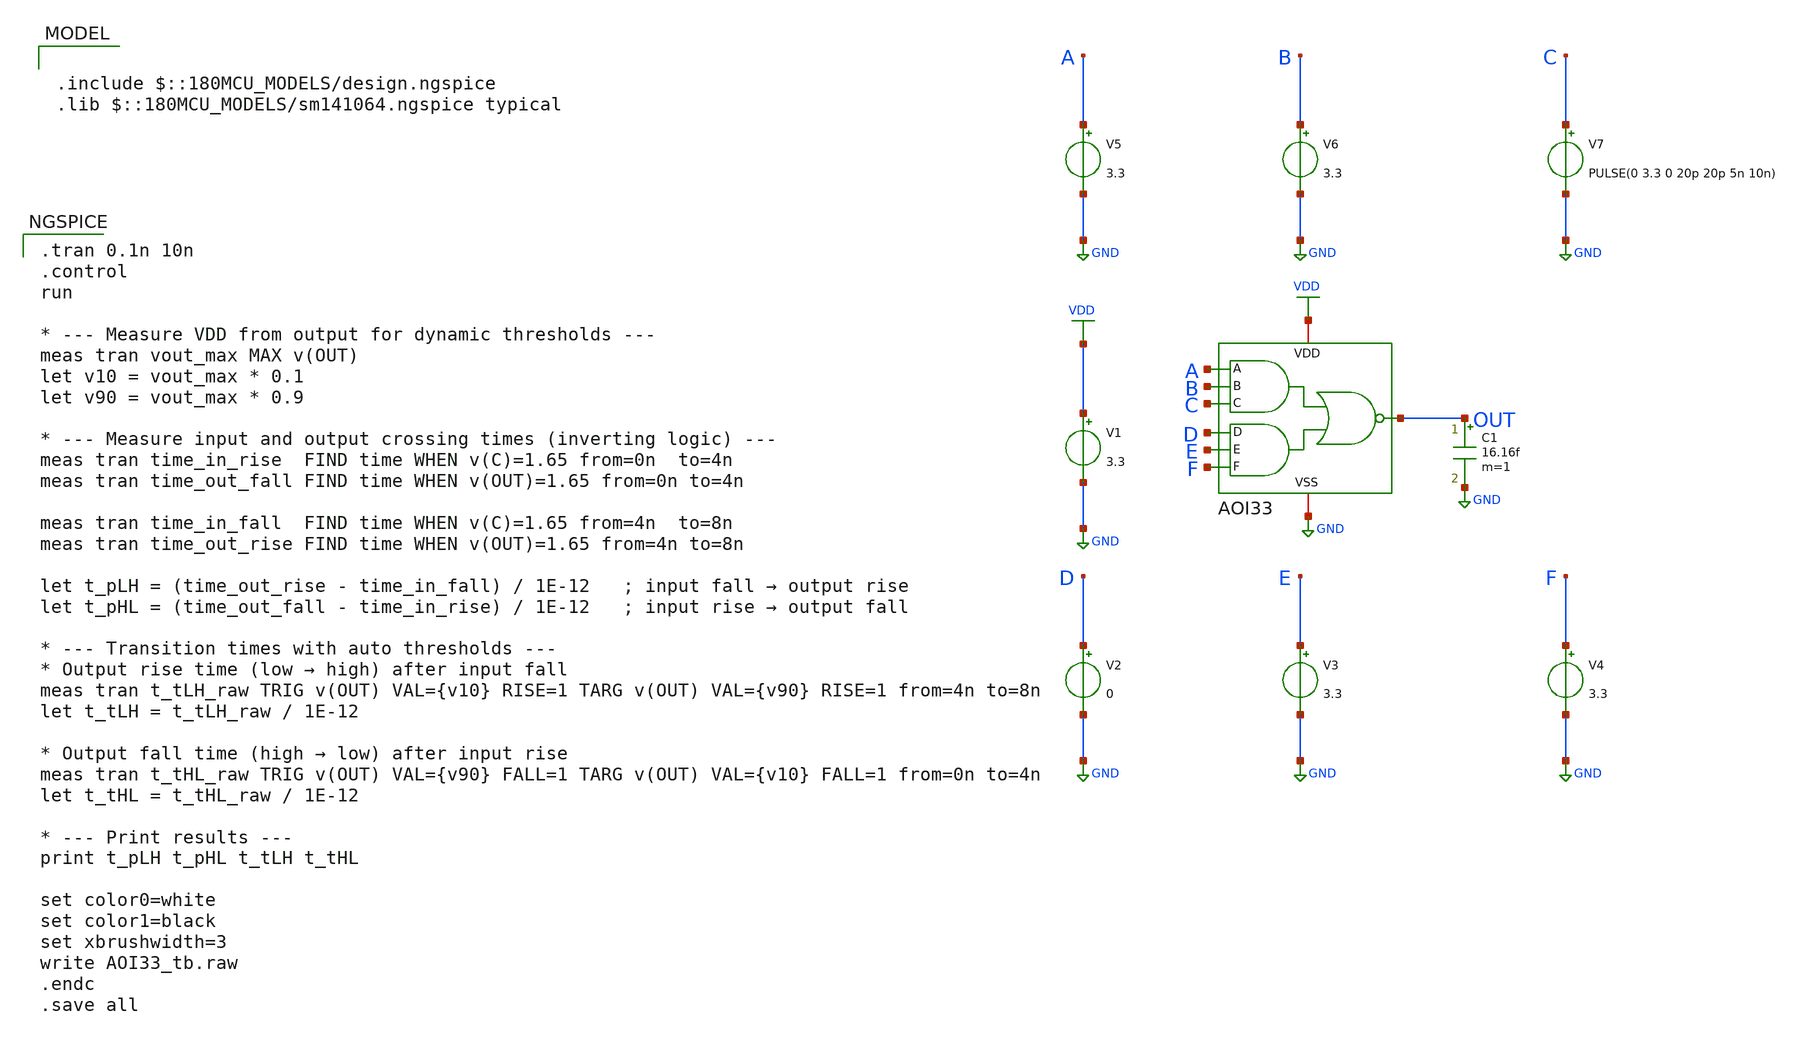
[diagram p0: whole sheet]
** sch_path: designs/AOI33/xschem/AOI33_tb.sch
**.subckt AOI33_tb
V1 VDD GND 3.3
V2 D GND 0
V3 E GND 3.3
V4 F GND 3.3
V5 A GND 3.3
V6 B GND 3.3
V7 C GND PULSE(0 3.3 0 20p 20p 5n 10n)
C1 OUT GND 16.16f m=1
x1 VDD C B A F E D OUT GND AOI33
**** begin user architecture code

.include $::180MCU_MODELS/design.ngspice
.lib $::180MCU_MODELS/sm141064.ngspice typical


.tran 0.1n 10n
.control
run

* --- Measure VDD from output for dynamic thresholds ---
meas tran vout_max MAX v(OUT)
let v10 = vout_max * 0.1
let v90 = vout_max * 0.9

* --- Measure input and output crossing times (inverting logic) ---
meas tran time_in_rise  FIND time WHEN v(C)=1.65 from=0n  to=4n
meas tran time_out_fall FIND time WHEN v(OUT)=1.65 from=0n to=4n

meas tran time_in_fall  FIND time WHEN v(C)=1.65 from=4n  to=8n
meas tran time_out_rise FIND time WHEN v(OUT)=1.65 from=4n to=8n

let t_pLH = (time_out_rise - time_in_fall) / 1E-12   ; input fall → output rise
let t_pHL = (time_out_fall - time_in_rise) / 1E-12   ; input rise → output fall

* --- Transition times with auto thresholds ---
* Output rise time (low → high) after input fall
meas tran t_tLH_raw TRIG v(OUT) VAL={v10} RISE=1 TARG v(OUT) VAL={v90} RISE=1 from=4n to=8n
let t_tLH = t_tLH_raw / 1E-12

* Output fall time (high → low) after input rise
meas tran t_tHL_raw TRIG v(OUT) VAL={v90} FALL=1 TARG v(OUT) VAL={v10} FALL=1 from=0n to=4n
let t_tHL = t_tHL_raw / 1E-12

* --- Print results ---
print t_pLH t_pHL t_tLH t_tHL

set color0=white
set color1=black
set xbrushwidth=3
write AOI33_tb.raw
.endc
.save all

**** end user architecture code
**.ends

* expanding   symbol:  chipabros/AOI33_CRIT/AOI33.sym # of pins=9
** sym_path: designs/AOI33/xschem/AOI33.sym
** sch_path: designs/AOI33/xschem/AOI33.sch
.subckt AOI33 VDD C B A F E D OUT VSS
*.iopin VSS
*.iopin VDD
*.ipin A
*.ipin D
*.ipin E
*.ipin B
*.ipin C
*.ipin F
*.opin OUT
XM1 OUT A net1 VSS nfet_03v3 L=0.3u W=2.55u nf=1 ad='int((nf+1)/2) * W/nf * 0.18u' as='int((nf+2)/2) * W/nf * 0.18u'
+ pd='2*int((nf+1)/2) * (W/nf + 0.18u)' ps='2*int((nf+2)/2) * (W/nf + 0.18u)' nrd='0.18u / W' nrs='0.18u / W'
+ sa=0 sb=0 sd=0 m=1
XM7 net5 A VDD VDD pfet_03v3 L=0.3u W=3.4u nf=1 ad='int((nf+1)/2) * W/nf * 0.18u' as='int((nf+2)/2) * W/nf * 0.18u'
+ pd='2*int((nf+1)/2) * (W/nf + 0.18u)' ps='2*int((nf+2)/2) * (W/nf + 0.18u)' nrd='0.18u / W' nrs='0.18u / W'
+ sa=0 sb=0 sd=0 m=1
XM2 net1 B net2 VSS nfet_03v3 L=0.3u W=2.55u nf=1 ad='int((nf+1)/2) * W/nf * 0.18u' as='int((nf+2)/2) * W/nf * 0.18u'
+ pd='2*int((nf+1)/2) * (W/nf + 0.18u)' ps='2*int((nf+2)/2) * (W/nf + 0.18u)' nrd='0.18u / W' nrs='0.18u / W'
+ sa=0 sb=0 sd=0 m=1
XM3 net2 C VSS VSS nfet_03v3 L=0.3u W=2.55u nf=1 ad='int((nf+1)/2) * W/nf * 0.18u' as='int((nf+2)/2) * W/nf * 0.18u'
+ pd='2*int((nf+1)/2) * (W/nf + 0.18u)' ps='2*int((nf+2)/2) * (W/nf + 0.18u)' nrd='0.18u / W' nrs='0.18u / W'
+ sa=0 sb=0 sd=0 m=1
XM4 OUT D net4 VSS nfet_03v3 L=0.3u W=2.55u nf=1 ad='int((nf+1)/2) * W/nf * 0.18u' as='int((nf+2)/2) * W/nf * 0.18u'
+ pd='2*int((nf+1)/2) * (W/nf + 0.18u)' ps='2*int((nf+2)/2) * (W/nf + 0.18u)' nrd='0.18u / W' nrs='0.18u / W'
+ sa=0 sb=0 sd=0 m=1
XM5 net4 E net3 VSS nfet_03v3 L=0.3u W=2.55u nf=1 ad='int((nf+1)/2) * W/nf * 0.18u' as='int((nf+2)/2) * W/nf * 0.18u'
+ pd='2*int((nf+1)/2) * (W/nf + 0.18u)' ps='2*int((nf+2)/2) * (W/nf + 0.18u)' nrd='0.18u / W' nrs='0.18u / W'
+ sa=0 sb=0 sd=0 m=1
XM6 net3 F VSS VSS nfet_03v3 L=0.3u W=2.55u nf=1 ad='int((nf+1)/2) * W/nf * 0.18u' as='int((nf+2)/2) * W/nf * 0.18u'
+ pd='2*int((nf+1)/2) * (W/nf + 0.18u)' ps='2*int((nf+2)/2) * (W/nf + 0.18u)' nrd='0.18u / W' nrs='0.18u / W'
+ sa=0 sb=0 sd=0 m=1
XM8 net5 B VDD VDD pfet_03v3 L=0.3u W=3.4u nf=1 ad='int((nf+1)/2) * W/nf * 0.18u' as='int((nf+2)/2) * W/nf * 0.18u'
+ pd='2*int((nf+1)/2) * (W/nf + 0.18u)' ps='2*int((nf+2)/2) * (W/nf + 0.18u)' nrd='0.18u / W' nrs='0.18u / W'
+ sa=0 sb=0 sd=0 m=1
XM9 net5 C VDD VDD pfet_03v3 L=0.3u W=3.4u nf=1 ad='int((nf+1)/2) * W/nf * 0.18u' as='int((nf+2)/2) * W/nf * 0.18u'
+ pd='2*int((nf+1)/2) * (W/nf + 0.18u)' ps='2*int((nf+2)/2) * (W/nf + 0.18u)' nrd='0.18u / W' nrs='0.18u / W'
+ sa=0 sb=0 sd=0 m=1
XM10 OUT D net5 VDD pfet_03v3 L=0.3u W=3.4u nf=1 ad='int((nf+1)/2) * W/nf * 0.18u' as='int((nf+2)/2) * W/nf * 0.18u'
+ pd='2*int((nf+1)/2) * (W/nf + 0.18u)' ps='2*int((nf+2)/2) * (W/nf + 0.18u)' nrd='0.18u / W' nrs='0.18u / W'
+ sa=0 sb=0 sd=0 m=1
XM11 OUT E net5 VDD pfet_03v3 L=0.3u W=3.4u nf=1 ad='int((nf+1)/2) * W/nf * 0.18u' as='int((nf+2)/2) * W/nf * 0.18u'
+ pd='2*int((nf+1)/2) * (W/nf + 0.18u)' ps='2*int((nf+2)/2) * (W/nf + 0.18u)' nrd='0.18u / W' nrs='0.18u / W'
+ sa=0 sb=0 sd=0 m=1
XM12 OUT F net5 VDD pfet_03v3 L=0.3u W=3.4u nf=1 ad='int((nf+1)/2) * W/nf * 0.18u' as='int((nf+2)/2) * W/nf * 0.18u'
+ pd='2*int((nf+1)/2) * (W/nf + 0.18u)' ps='2*int((nf+2)/2) * (W/nf + 0.18u)' nrd='0.18u / W' nrs='0.18u / W'
+ sa=0 sb=0 sd=0 m=1
.ends

.GLOBAL VDD
.GLOBAL GND
.end
